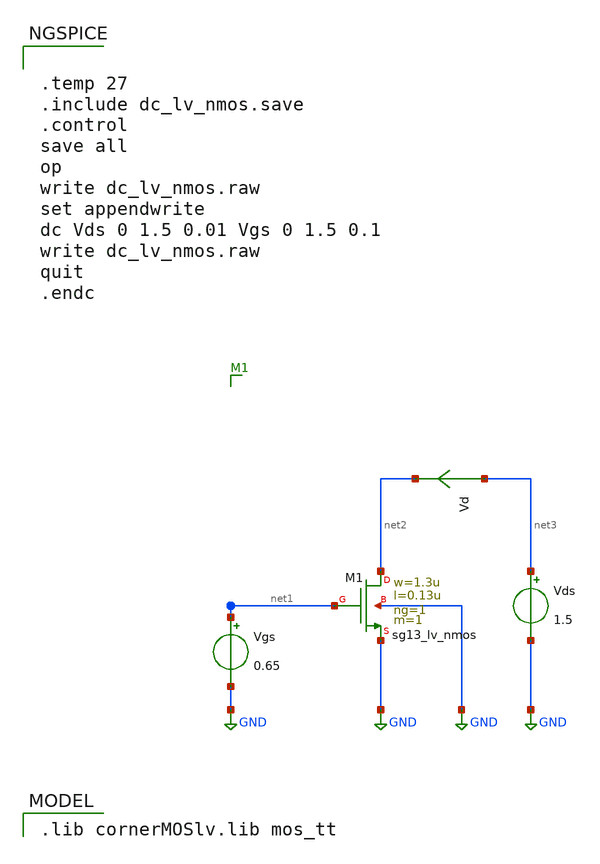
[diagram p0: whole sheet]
** sch_path: xschem/dc_lv_nmos.sch
* (c) 2023-2025 Harald Pretl, Apache-2.0 license
**.subckt dc_lv_nmos
Vgs net1 GND 0.65
Vds net3 GND 1.5
XM1 net2 net1 GND GND sg13_lv_nmos w=1.3u l=0.13u ng=1 m=1 mm_ok=1
Vd net3 net2 0
.save i(vd)
**** begin user architecture code
 .lib cornerMOSlv.lib mos_tt



.temp 27
.include dc_lv_nmos.save
.control
save all
op
write dc_lv_nmos.raw
set appendwrite
dc Vds 0 1.5 0.01 Vgs 0 1.5 0.1
write dc_lv_nmos.raw
quit
.endc


**** end user architecture code
**.ends
.GLOBAL GND
.end
